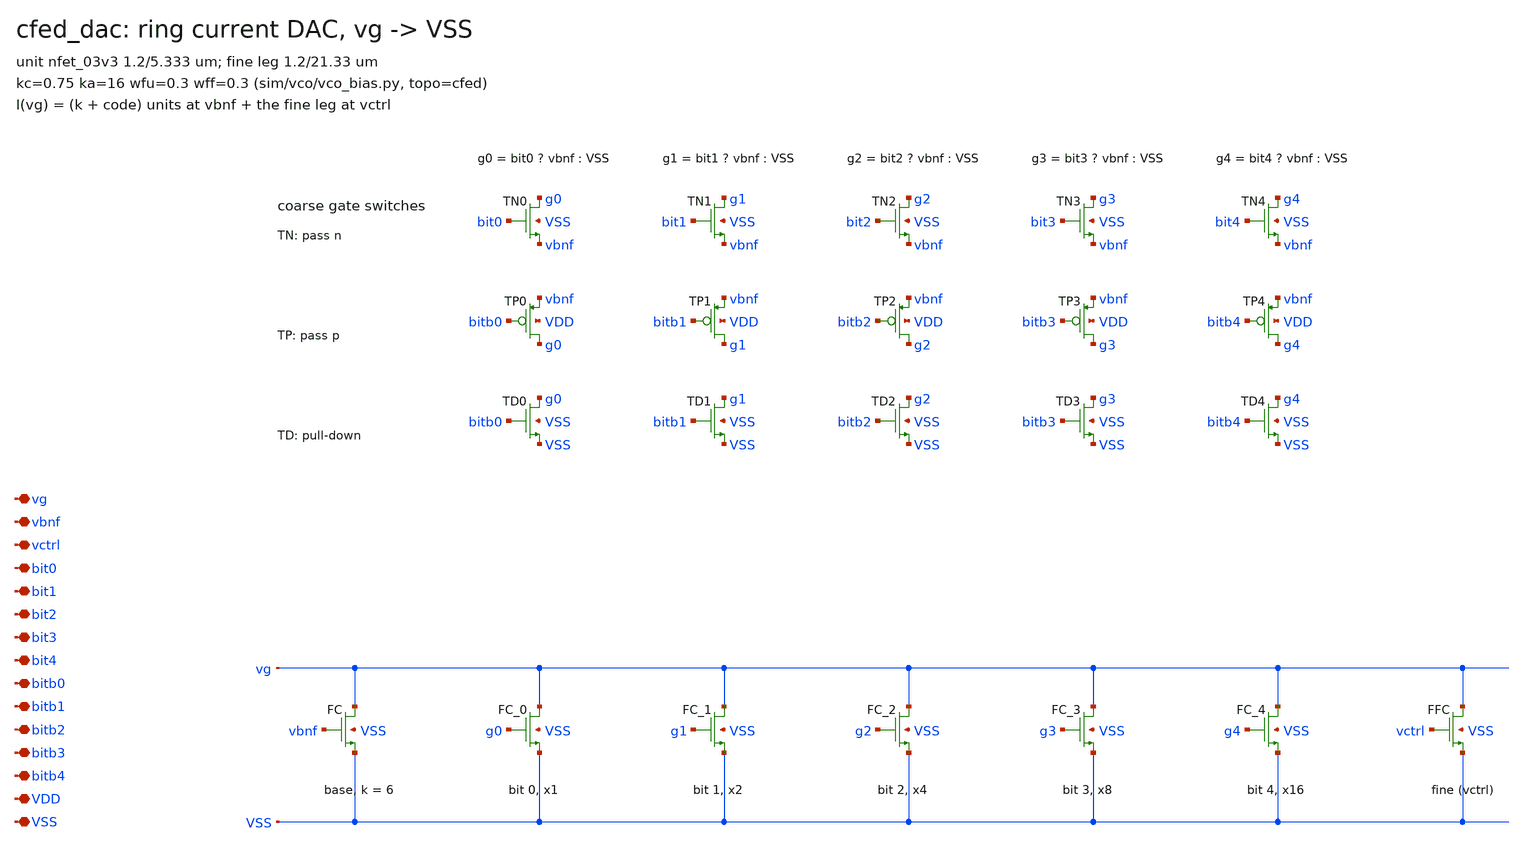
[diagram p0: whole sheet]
** sch_path: xschem/cfed_dac.sch
**.subckt cfed_dac vg vbnf vctrl bit0 bit1 bit2 bit3 bit4 bitb0 bitb1 bitb2 bitb3 bitb4 VDD VSS
*.iopin vg
*.iopin vbnf
*.iopin vctrl
*.iopin bit0
*.iopin bit1
*.iopin bit2
*.iopin bit3
*.iopin bit4
*.iopin bitb0
*.iopin bitb1
*.iopin bitb2
*.iopin bitb3
*.iopin bitb4
*.iopin VDD
*.iopin VSS
XFC vg vbnf VSS VSS nfet_03v3 L=5.333333333333333u W=1.2u nf=1 ad=0.6p as=0.6p pd=3.4u ps=3.4u nrd=0
+ nrs=0 sa=0 sb=0 sd=0 m=6
XFC_0 vg g0 VSS VSS nfet_03v3 L=5.333333333333333u W=1.2u nf=1 ad=0.6p as=0.6p pd=3.4u ps=3.4u nrd=0
+ nrs=0 sa=0 sb=0 sd=0 m=1
XFC_1 vg g1 VSS VSS nfet_03v3 L=5.333333333333333u W=1.2u nf=1 ad=0.6p as=0.6p pd=3.4u ps=3.4u nrd=0
+ nrs=0 sa=0 sb=0 sd=0 m=2
XFC_2 vg g2 VSS VSS nfet_03v3 L=5.333333333333333u W=1.2u nf=1 ad=0.6p as=0.6p pd=3.4u ps=3.4u nrd=0
+ nrs=0 sa=0 sb=0 sd=0 m=4
XFC_3 vg g3 VSS VSS nfet_03v3 L=5.333333333333333u W=1.2u nf=1 ad=0.6p as=0.6p pd=3.4u ps=3.4u nrd=0
+ nrs=0 sa=0 sb=0 sd=0 m=8
XFC_4 vg g4 VSS VSS nfet_03v3 L=5.333333333333333u W=1.2u nf=1 ad=0.6p as=0.6p pd=3.4u ps=3.4u nrd=0
+ nrs=0 sa=0 sb=0 sd=0 m=16
XFFC vg vctrl VSS VSS nfet_03v3 L=21.333333333333332u W=1.2u nf=1 ad=0.6p as=0.6p pd=3.4u ps=3.4u
+ nrd=0 nrs=0 sa=0 sb=0 sd=0 m=1
XTN0 g0 bit0 vbnf VSS nfet_03v3 L=0.28u W=2.0u nf=1 ad=1.0p as=1.0p pd=5.0u ps=5.0u nrd=0 nrs=0 sa=0
+ sb=0 sd=0 m=1
XTP0 g0 bitb0 vbnf VDD pfet_03v3 L=0.28u W=5.0u nf=1 ad=2.5p as=2.5p pd=11.0u ps=11.0u nrd=0 nrs=0
+ sa=0 sb=0 sd=0 m=1
XTD0 g0 bitb0 VSS VSS nfet_03v3 L=0.28u W=1.0u nf=1 ad=0.5p as=0.5p pd=3.0u ps=3.0u nrd=0 nrs=0 sa=0
+ sb=0 sd=0 m=1
XTN1 g1 bit1 vbnf VSS nfet_03v3 L=0.28u W=2.0u nf=1 ad=1.0p as=1.0p pd=5.0u ps=5.0u nrd=0 nrs=0 sa=0
+ sb=0 sd=0 m=1
XTP1 g1 bitb1 vbnf VDD pfet_03v3 L=0.28u W=5.0u nf=1 ad=2.5p as=2.5p pd=11.0u ps=11.0u nrd=0 nrs=0
+ sa=0 sb=0 sd=0 m=1
XTD1 g1 bitb1 VSS VSS nfet_03v3 L=0.28u W=1.0u nf=1 ad=0.5p as=0.5p pd=3.0u ps=3.0u nrd=0 nrs=0 sa=0
+ sb=0 sd=0 m=1
XTN2 g2 bit2 vbnf VSS nfet_03v3 L=0.28u W=2.0u nf=1 ad=1.0p as=1.0p pd=5.0u ps=5.0u nrd=0 nrs=0 sa=0
+ sb=0 sd=0 m=1
XTP2 g2 bitb2 vbnf VDD pfet_03v3 L=0.28u W=5.0u nf=1 ad=2.5p as=2.5p pd=11.0u ps=11.0u nrd=0 nrs=0
+ sa=0 sb=0 sd=0 m=1
XTD2 g2 bitb2 VSS VSS nfet_03v3 L=0.28u W=1.0u nf=1 ad=0.5p as=0.5p pd=3.0u ps=3.0u nrd=0 nrs=0 sa=0
+ sb=0 sd=0 m=1
XTN3 g3 bit3 vbnf VSS nfet_03v3 L=0.28u W=2.0u nf=1 ad=1.0p as=1.0p pd=5.0u ps=5.0u nrd=0 nrs=0 sa=0
+ sb=0 sd=0 m=1
XTP3 g3 bitb3 vbnf VDD pfet_03v3 L=0.28u W=5.0u nf=1 ad=2.5p as=2.5p pd=11.0u ps=11.0u nrd=0 nrs=0
+ sa=0 sb=0 sd=0 m=1
XTD3 g3 bitb3 VSS VSS nfet_03v3 L=0.28u W=1.0u nf=1 ad=0.5p as=0.5p pd=3.0u ps=3.0u nrd=0 nrs=0 sa=0
+ sb=0 sd=0 m=1
XTN4 g4 bit4 vbnf VSS nfet_03v3 L=0.28u W=2.0u nf=1 ad=1.0p as=1.0p pd=5.0u ps=5.0u nrd=0 nrs=0 sa=0
+ sb=0 sd=0 m=1
XTP4 g4 bitb4 vbnf VDD pfet_03v3 L=0.28u W=5.0u nf=1 ad=2.5p as=2.5p pd=11.0u ps=11.0u nrd=0 nrs=0
+ sa=0 sb=0 sd=0 m=1
XTD4 g4 bitb4 VSS VSS nfet_03v3 L=0.28u W=1.0u nf=1 ad=0.5p as=0.5p pd=3.0u ps=3.0u nrd=0 nrs=0 sa=0
+ sb=0 sd=0 m=1
**.ends
.end
